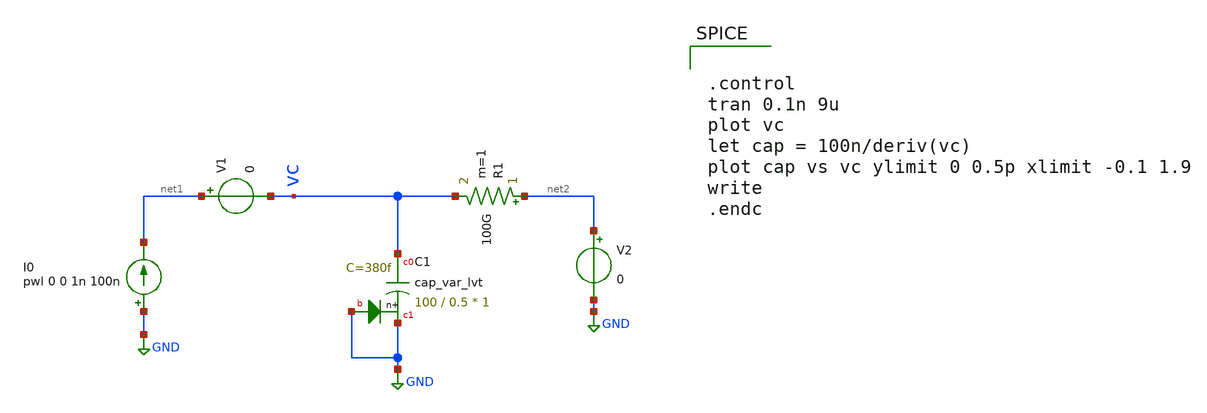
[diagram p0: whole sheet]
** sch_path: varactor_meas/varactor_tran.sch
**.subckt varactor_tran
XC1 vc GND GND sky130_fd_pr__cap_var_lvt W=100 L=0.5 VM=1 m=1
I0 GND net1 pwl 0 0 1n 100n
V1 net1 vc 0
R1 net2 vc 100G m=1
V2 net2 GND 0
**** begin user architecture code


.control
tran 0.1n 9u
plot vc
let cap = 100n/deriv(vc)
plot cap vs vc ylimit 0 0.5p xlimit -0.1 1.9
write
.endc




.option wnflag = 1
.lib /usr/local/share/pdk/sky130A/libs.tech/ngspice/sky130.lib.spice tt
.include /usr/local/share/pdk/sky130A/libs.ref/sky130_fd_pr/spice/sky130_fd_pr__ind_05_220.model.spice
.param mc_mm_switch=0


**** end user architecture code
**.ends
.GLOBAL GND
.end
